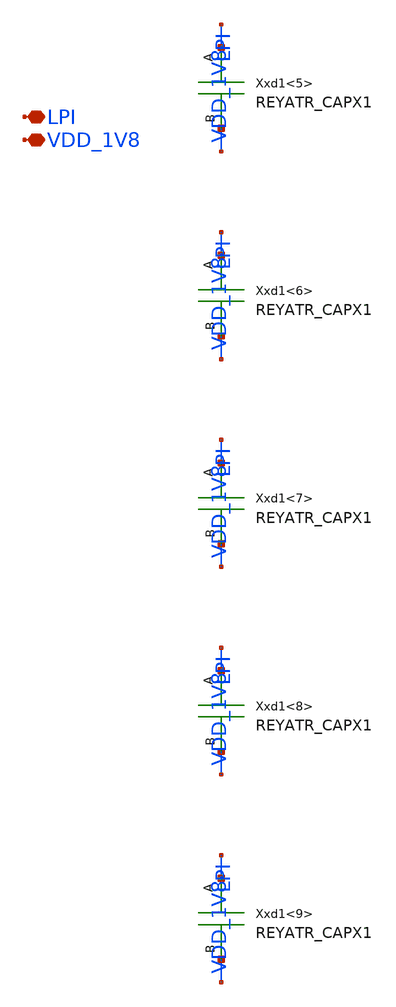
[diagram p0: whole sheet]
** sch_path: design/LELO_TEMP_SKY130A/LELOTEMP_BIAS_IBP_CAP_LPI_B.sch
**.subckt LELOTEMP_BIAS_IBP_CAP_LPI_B LPI VDD_1V8
*.iopin LPI
*.iopin VDD_1V8
Xxd1<5> LPI VDD_1V8 REYATR_CAPX1
Xxd1<6> LPI VDD_1V8 REYATR_CAPX1
Xxd1<7> LPI VDD_1V8 REYATR_CAPX1
Xxd1<8> LPI VDD_1V8 REYATR_CAPX1
Xxd1<9> LPI VDD_1V8 REYATR_CAPX1
**.ends

* expanding   symbol:  REY_ATR_SKY130A/REYATR_CAPX1.sym # of pins=2
** sym_path: design/LELO_TEMP_SKY130A/REYATR_CAPX1.sym
** sch_path: design/LELO_TEMP_SKY130A/REYATR_CAPX1.sch
.subckt REYATR_CAPX1 A B
*.iopin A
*.iopin B
XC1 B A sky130_fd_pr__cap_mim_m3_1 W=4.8 L=5 MF=1 m=1
.ends

.end
